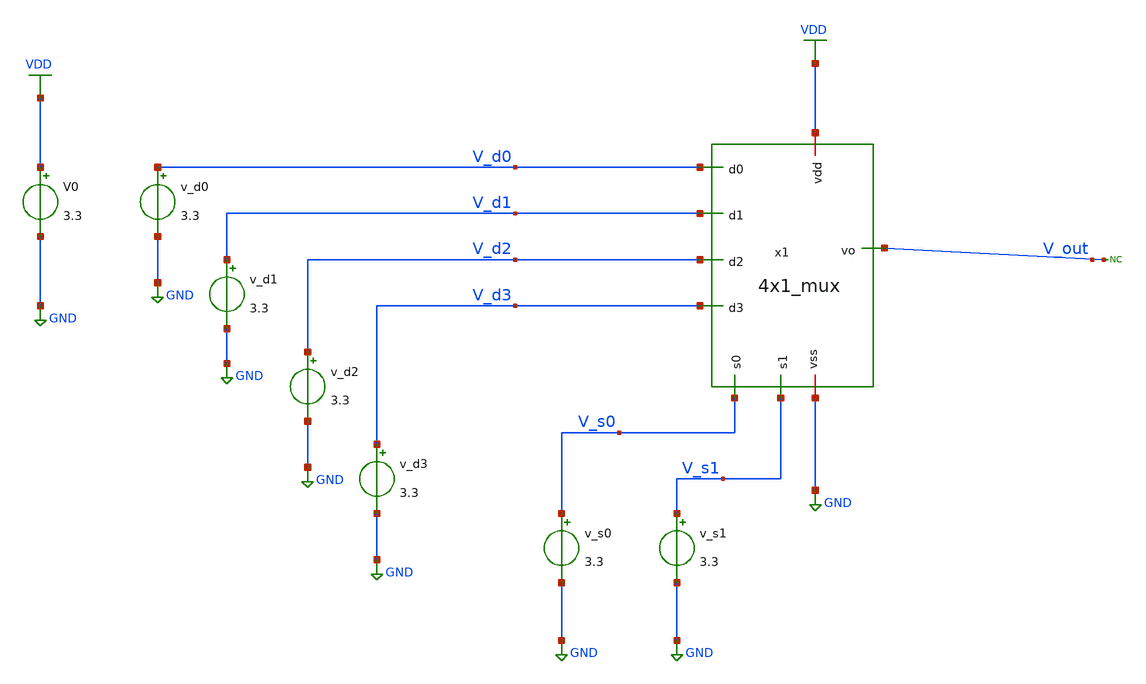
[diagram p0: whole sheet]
** sch_path: designs/4x1_mux_tb.sch
**.subckt 4x1_mux_tb
x1 V_s1 V_s0 VDD V_d0 V_d1 net1 V_d2 V_d3 GND 4x1_mux
v_d0 V_d0 GND 3.3
v_d1 V_d1 GND 3.3
v_d2 V_d2 GND 3.3
v_d3 V_d3 GND 3.3
v_s0 V_s0 GND 3.3
v_s1 V_s1 GND 3.3
V0 VDD GND 3.3
* noconn #net1
**** begin user architecture code


.control
save all

* Define transient params for 4 inputs (2^4 = 16 states)
let t_base = 20n
* Run for 160ns to see all 16 states
let tstop = 8 * t_base
let tstep = t_base / 1000

* Override schematic DC sources with PULSE definitions
alter @VIN0[PULSE] = [ 0 3.3 0 100p 100p   9.9n  20n ]
alter @VIN1[PULSE] = [ 0 3.3 0 100p 100p  19.9n  40n ]
alter @VIN2[PULSE] = [ 0 3.3 0 100p 100p  39.9n  80n ]
alter @VIN3[PULSE] = [ 0 3.3 0 100p 100p  79.9n 160n ]

* Simulations
op
tran $&tstep $&tstop

* Plots
setplot tran1
let vin0 = v(vin0)
let vin1 = v(vin1)
let vin2 = v(vin2)
let vin3 = v(vin3)
let vout = v(vout)
* Supply current in mA
let ivdd = -v1#branch * 1m

plot v(vout) v(vin0)+4 v(vin1)+8 v(vin2)+12 v(vin3)+16 title '4-Input OR Gate Response'

.endc



.include $::180MCU_MODELS/design.ngspice
.lib $::180MCU_MODELS/sm141064.ngspice typical

**** end user architecture code
**.ends

* expanding   symbol:  4x1_mux.sym # of pins=9
** sym_path: designs/4x1_mux.sym
** sch_path: designs/4x1_mux.sch
.subckt 4x1_mux s1 s0 vdd d0 d1 vo d2 d3 vss
*.ipin d0
*.ipin d1
*.ipin d2
*.ipin d3
*.ipin s1
*.ipin s0
*.iopin vdd
*.iopin vss
*.opin vo
x1 vdd net3 d0 net2 net1 vss 3_input_and
x2 vdd net4 d1 net2 s0 vss 3_input_and
x3 vdd net5 d2 s1 net1 vss 3_input_and
x4 vdd net6 d3 s1 s0 vss 3_input_and
x5 vdd net3 net4 net5 net6 vo vss 4_input_or
x6 vdd s1 net2 vss inv
x7 vdd s0 net1 vss inv
.ends


* expanding   symbol:  3_input_and.sym # of pins=6
** sym_path: designs/3_input_and.sym
** sch_path: designs/3_input_and.sch
.subckt 3_input_and vdd Vo Vi_1 Vi_2 Vi_3 vss
*.iopin vdd
*.iopin vss
*.ipin Vi_1
*.ipin Vi_2
*.ipin Vi_3
*.opin Vo
XM1 net1 Vi_1 vdd vdd pfet_03v3 L=0.28u W=0.22u nf=1 ad='int((nf+1)/2) * W/nf * 0.18u' as='int((nf+2)/2) * W/nf * 0.18u'
+ pd='2*int((nf+1)/2) * (W/nf + 0.18u)' ps='2*int((nf+2)/2) * (W/nf + 0.18u)' nrd='0.18u / W' nrs='0.18u / W'
+ sa=0 sb=0 sd=0 m=1
XM2 net1 Vi_2 vdd vdd pfet_03v3 L=0.28u W=0.22u nf=1 ad='int((nf+1)/2) * W/nf * 0.18u' as='int((nf+2)/2) * W/nf * 0.18u'
+ pd='2*int((nf+1)/2) * (W/nf + 0.18u)' ps='2*int((nf+2)/2) * (W/nf + 0.18u)' nrd='0.18u / W' nrs='0.18u / W'
+ sa=0 sb=0 sd=0 m=1
XM3 net1 Vi_3 vdd vdd pfet_03v3 L=0.28u W=0.22u nf=1 ad='int((nf+1)/2) * W/nf * 0.18u' as='int((nf+2)/2) * W/nf * 0.18u'
+ pd='2*int((nf+1)/2) * (W/nf + 0.18u)' ps='2*int((nf+2)/2) * (W/nf + 0.18u)' nrd='0.18u / W' nrs='0.18u / W'
+ sa=0 sb=0 sd=0 m=1
XM4 net1 Vi_1 net3 vss nfet_03v3 L=0.28u W=0.22u nf=1 ad='int((nf+1)/2) * W/nf * 0.18u' as='int((nf+2)/2) * W/nf * 0.18u'
+ pd='2*int((nf+1)/2) * (W/nf + 0.18u)' ps='2*int((nf+2)/2) * (W/nf + 0.18u)' nrd='0.18u / W' nrs='0.18u / W'
+ sa=0 sb=0 sd=0 m=1
XM5 net3 Vi_2 net2 vss nfet_03v3 L=0.28u W=0.22u nf=1 ad='int((nf+1)/2) * W/nf * 0.18u' as='int((nf+2)/2) * W/nf * 0.18u'
+ pd='2*int((nf+1)/2) * (W/nf + 0.18u)' ps='2*int((nf+2)/2) * (W/nf + 0.18u)' nrd='0.18u / W' nrs='0.18u / W'
+ sa=0 sb=0 sd=0 m=1
XM6 net2 Vi_3 vss vss nfet_03v3 L=0.28u W=0.22u nf=1 ad='int((nf+1)/2) * W/nf * 0.18u' as='int((nf+2)/2) * W/nf * 0.18u'
+ pd='2*int((nf+1)/2) * (W/nf + 0.18u)' ps='2*int((nf+2)/2) * (W/nf + 0.18u)' nrd='0.18u / W' nrs='0.18u / W'
+ sa=0 sb=0 sd=0 m=1
XM7 Vo net1 vdd vdd pfet_03v3 L=0.28u W=0.22u nf=1 ad='int((nf+1)/2) * W/nf * 0.18u' as='int((nf+2)/2) * W/nf * 0.18u'
+ pd='2*int((nf+1)/2) * (W/nf + 0.18u)' ps='2*int((nf+2)/2) * (W/nf + 0.18u)' nrd='0.18u / W' nrs='0.18u / W'
+ sa=0 sb=0 sd=0 m=1
XM8 Vo net1 vss vss nfet_03v3 L=0.28u W=0.22u nf=1 ad='int((nf+1)/2) * W/nf * 0.18u' as='int((nf+2)/2) * W/nf * 0.18u'
+ pd='2*int((nf+1)/2) * (W/nf + 0.18u)' ps='2*int((nf+2)/2) * (W/nf + 0.18u)' nrd='0.18u / W' nrs='0.18u / W'
+ sa=0 sb=0 sd=0 m=1
.ends


* expanding   symbol:  4_input_or.sym # of pins=7
** sym_path: designs/4_input_or.sym
** sch_path: designs/4_input_or.sch
.subckt 4_input_or vdd vin_0 vin_1 vin_2 vin_3 vout vss
*.iopin vdd
*.iopin vss
*.ipin vin_0
*.ipin vin_1
*.ipin vin_2
*.ipin vin_3
*.opin vout
XM1 net1 vin_0 vdd vdd pfet_03v3 L=0.28u W=0.22u nf=1 ad='int((nf+1)/2) * W/nf * 0.18u' as='int((nf+2)/2) * W/nf * 0.18u'
+ pd='2*int((nf+1)/2) * (W/nf + 0.18u)' ps='2*int((nf+2)/2) * (W/nf + 0.18u)' nrd='0.18u / W' nrs='0.18u / W'
+ sa=0 sb=0 sd=0 m=1
XM2 net4 vin_3 vss vss nfet_03v3 L=0.28u W=0.22u nf=1 ad='int((nf+1)/2) * W/nf * 0.18u' as='int((nf+2)/2) * W/nf * 0.18u'
+ pd='2*int((nf+1)/2) * (W/nf + 0.18u)' ps='2*int((nf+2)/2) * (W/nf + 0.18u)' nrd='0.18u / W' nrs='0.18u / W'
+ sa=0 sb=0 sd=0 m=1
XM3 net2 vin_1 net1 vdd pfet_03v3 L=0.28u W=0.22u nf=1 ad='int((nf+1)/2) * W/nf * 0.18u' as='int((nf+2)/2) * W/nf * 0.18u'
+ pd='2*int((nf+1)/2) * (W/nf + 0.18u)' ps='2*int((nf+2)/2) * (W/nf + 0.18u)' nrd='0.18u / W' nrs='0.18u / W'
+ sa=0 sb=0 sd=0 m=1
XM4 net3 vin_2 net2 vdd pfet_03v3 L=0.28u W=0.22u nf=1 ad='int((nf+1)/2) * W/nf * 0.18u' as='int((nf+2)/2) * W/nf * 0.18u'
+ pd='2*int((nf+1)/2) * (W/nf + 0.18u)' ps='2*int((nf+2)/2) * (W/nf + 0.18u)' nrd='0.18u / W' nrs='0.18u / W'
+ sa=0 sb=0 sd=0 m=1
XM5 net4 vin_3 net3 vdd pfet_03v3 L=0.28u W=0.22u nf=1 ad='int((nf+1)/2) * W/nf * 0.18u' as='int((nf+2)/2) * W/nf * 0.18u'
+ pd='2*int((nf+1)/2) * (W/nf + 0.18u)' ps='2*int((nf+2)/2) * (W/nf + 0.18u)' nrd='0.18u / W' nrs='0.18u / W'
+ sa=0 sb=0 sd=0 m=1
XM6 net4 vin_2 vss vss nfet_03v3 L=0.28u W=0.22u nf=1 ad='int((nf+1)/2) * W/nf * 0.18u' as='int((nf+2)/2) * W/nf * 0.18u'
+ pd='2*int((nf+1)/2) * (W/nf + 0.18u)' ps='2*int((nf+2)/2) * (W/nf + 0.18u)' nrd='0.18u / W' nrs='0.18u / W'
+ sa=0 sb=0 sd=0 m=1
XM7 net4 vin_1 vss vss nfet_03v3 L=0.28u W=0.22u nf=1 ad='int((nf+1)/2) * W/nf * 0.18u' as='int((nf+2)/2) * W/nf * 0.18u'
+ pd='2*int((nf+1)/2) * (W/nf + 0.18u)' ps='2*int((nf+2)/2) * (W/nf + 0.18u)' nrd='0.18u / W' nrs='0.18u / W'
+ sa=0 sb=0 sd=0 m=1
XM8 net4 vin_0 vss vss nfet_03v3 L=0.28u W=0.22u nf=1 ad='int((nf+1)/2) * W/nf * 0.18u' as='int((nf+2)/2) * W/nf * 0.18u'
+ pd='2*int((nf+1)/2) * (W/nf + 0.18u)' ps='2*int((nf+2)/2) * (W/nf + 0.18u)' nrd='0.18u / W' nrs='0.18u / W'
+ sa=0 sb=0 sd=0 m=1
XM9 vout net4 vdd vdd pfet_03v3 L=0.28u W=0.22u nf=1 ad='int((nf+1)/2) * W/nf * 0.18u' as='int((nf+2)/2) * W/nf * 0.18u'
+ pd='2*int((nf+1)/2) * (W/nf + 0.18u)' ps='2*int((nf+2)/2) * (W/nf + 0.18u)' nrd='0.18u / W' nrs='0.18u / W'
+ sa=0 sb=0 sd=0 m=1
XM10 vout net4 vss vss nfet_03v3 L=0.28u W=0.22u nf=1 ad='int((nf+1)/2) * W/nf * 0.18u' as='int((nf+2)/2) * W/nf * 0.18u'
+ pd='2*int((nf+1)/2) * (W/nf + 0.18u)' ps='2*int((nf+2)/2) * (W/nf + 0.18u)' nrd='0.18u / W' nrs='0.18u / W'
+ sa=0 sb=0 sd=0 m=1
.ends


* expanding   symbol:  inv.sym # of pins=4
** sym_path: designs/inv.sym
** sch_path: designs/inv.sch
.subckt inv vdd vin vout vss
*.iopin vdd
*.iopin vss
*.ipin vin
*.opin vout
XM1 vout vin vdd vdd pfet_03v3 L=0.28u W=0.22u nf=1 ad='int((nf+1)/2) * W/nf * 0.18u' as='int((nf+2)/2) * W/nf * 0.18u'
+ pd='2*int((nf+1)/2) * (W/nf + 0.18u)' ps='2*int((nf+2)/2) * (W/nf + 0.18u)' nrd='0.18u / W' nrs='0.18u / W'
+ sa=0 sb=0 sd=0 m=1
XM2 vout vin vss vss nfet_03v3 L=0.28u W=0.22u nf=1 ad='int((nf+1)/2) * W/nf * 0.18u' as='int((nf+2)/2) * W/nf * 0.18u'
+ pd='2*int((nf+1)/2) * (W/nf + 0.18u)' ps='2*int((nf+2)/2) * (W/nf + 0.18u)' nrd='0.18u / W' nrs='0.18u / W'
+ sa=0 sb=0 sd=0 m=1
.ends

.GLOBAL VDD
.GLOBAL GND
.end
